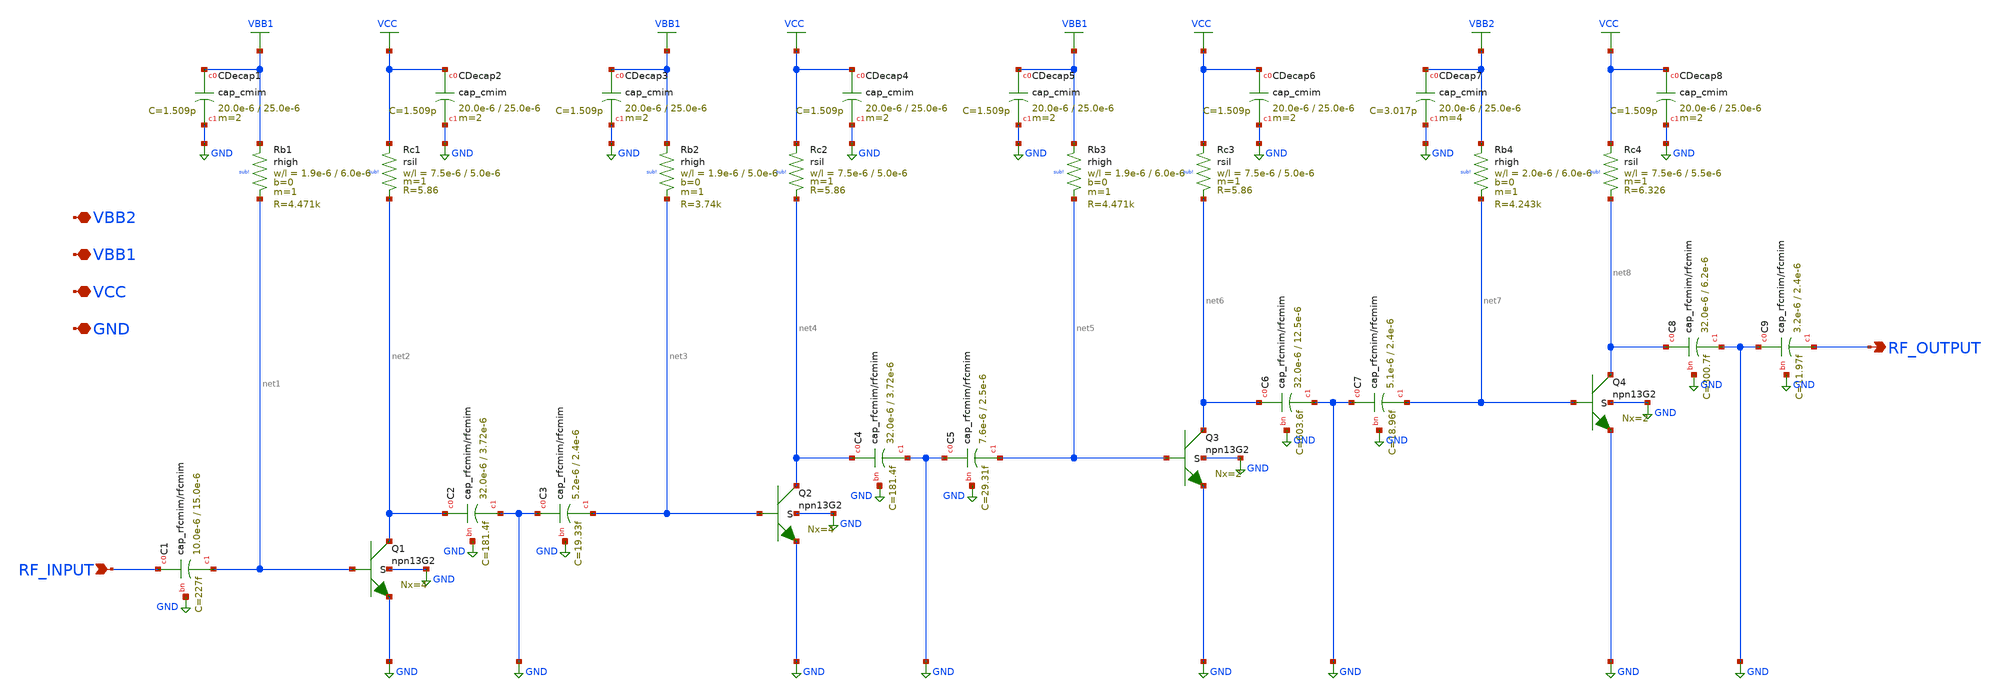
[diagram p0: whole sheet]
** sch_path: TO_Apr2025/160GHz_LNA/xschem/160GHz_LNA.sch
**.subckt 160GHz_LNA RF_INPUT GND VCC VBB1 RF_OUTPUT VBB2
*.ipin RF_INPUT
*.iopin GND
*.iopin VCC
*.iopin VBB1
*.opin RF_OUTPUT
*.iopin VBB2
XC1 RF_INPUT net1 GND cap_rfcmim w=10.0e-6 l=15.0e-6 wfeed=6.0e-6 m=1 mm_ok=1
XQ1 net2 net1 GND GND npn13G2 Nx=4 mm_ok=1
XRc1 VCC net2 sub! rsil w=7.5e-6 l=5.0e-6 m=1 mm_ok=1
XRb1 VBB1 net1 sub! rhigh w=1.9e-6 l=6.0e-6 m=1 b=0 mm_ok=1
XCDecap1 VBB1 GND cap_cmim w=20.0e-6 l=25.0e-6 m=2 mm_ok=1
XCDecap2 VCC GND cap_cmim w=20.0e-6 l=25.0e-6 m=2 mm_ok=1
XC2 net2 GND GND cap_rfcmim w=32.0e-6 l=3.72e-6 wfeed=3.0e-6 m=1 mm_ok=1
XC3 GND net3 GND cap_rfcmim w=5.2e-6 l=2.4e-6 wfeed=3.0e-6 m=1 mm_ok=1
XRb2 VBB1 net3 sub! rhigh w=1.9e-6 l=5.0e-6 m=1 b=0 mm_ok=1
XCDecap3 VBB1 GND cap_cmim w=20.0e-6 l=25.0e-6 m=2 mm_ok=1
XQ2 net4 net3 GND GND npn13G2 Nx=4 mm_ok=1
XRc2 VCC net4 sub! rsil w=7.5e-6 l=5.0e-6 m=1 mm_ok=1
XCDecap4 VCC GND cap_cmim w=20.0e-6 l=25.0e-6 m=2 mm_ok=1
XC4 net4 GND GND cap_rfcmim w=32.0e-6 l=3.72e-6 wfeed=3.0e-6 m=1 mm_ok=1
XC5 GND net5 GND cap_rfcmim w=7.6e-6 l=2.5e-6 wfeed=3.0e-6 m=1 mm_ok=1
XRb3 VBB1 net5 sub! rhigh w=1.9e-6 l=6.0e-6 m=1 b=0 mm_ok=1
XCDecap5 VBB1 GND cap_cmim w=20.0e-6 l=25.0e-6 m=2 mm_ok=1
XRc3 VCC net6 sub! rsil w=7.5e-6 l=5.0e-6 m=1 mm_ok=1
XCDecap6 VCC GND cap_cmim w=20.0e-6 l=25.0e-6 m=2 mm_ok=1
XQ3 net6 net5 GND GND npn13G2 Nx=2 mm_ok=1
XRb4 VBB2 net7 sub! rhigh w=2.0e-6 l=6.0e-6 m=1 b=0 mm_ok=1
XCDecap7 VBB2 GND cap_cmim w=20.0e-6 l=25.0e-6 m=4 mm_ok=1
XRc4 VCC net8 sub! rsil w=7.5e-6 l=5.5e-6 m=1 mm_ok=1
XCDecap8 VCC GND cap_cmim w=20.0e-6 l=25.0e-6 m=2 mm_ok=1
XQ4 net8 net7 GND GND npn13G2 Nx=2 mm_ok=1
XC6 net6 GND GND cap_rfcmim w=32.0e-6 l=12.5e-6 wfeed=3.0e-6 m=1 mm_ok=1
XC7 GND net7 GND cap_rfcmim w=5.1e-6 l=2.4e-6 wfeed=3.0e-6 m=1 mm_ok=1
XC8 net8 GND GND cap_rfcmim w=32.0e-6 l=6.2e-6 wfeed=3.0e-6 m=1 mm_ok=1
XC9 GND RF_OUTPUT GND cap_rfcmim w=3.2e-6 l=2.4e-6 wfeed=3.0e-6 m=1 mm_ok=1
**.ends
.end
